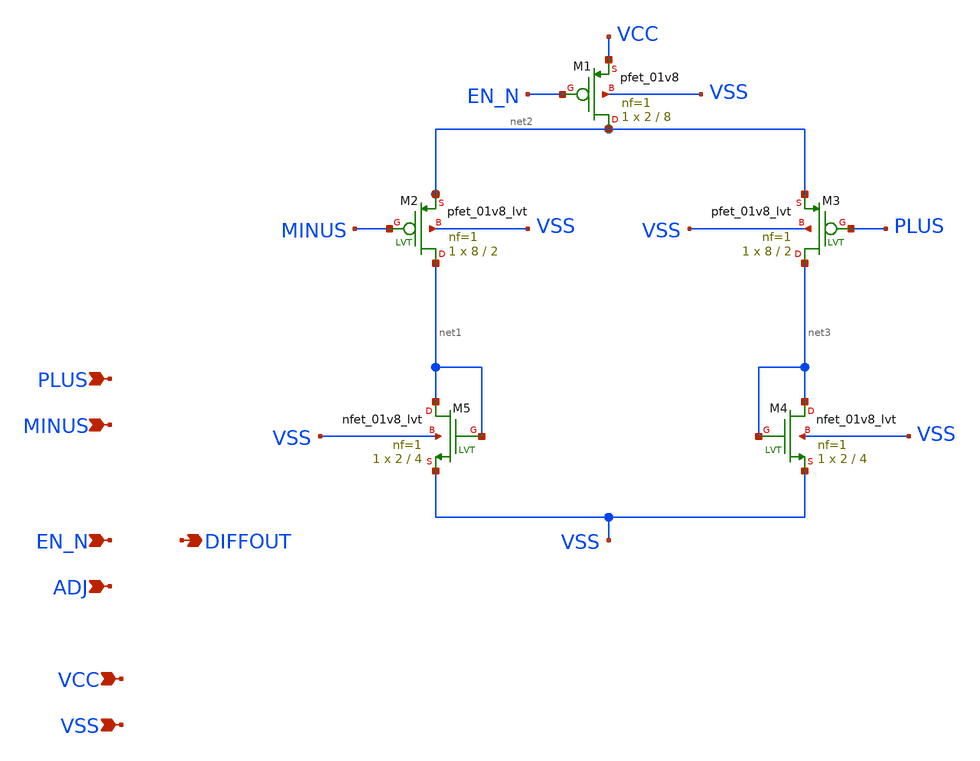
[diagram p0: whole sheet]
** sch_path: amplifier.sch
**.subckt amplifier PLUS MINUS VCC VSS EN_N ADJ DIFFOUT
*.ipin PLUS
*.ipin MINUS
*.ipin VCC
*.ipin VSS
*.ipin EN_N
*.ipin ADJ
*.opin DIFFOUT
XM1 net2 EN_N VCC VSS sky130_fd_pr__pfet_01v8 L=8 W=2 nf=1 ad='int((nf+1)/2) * W/nf * 0.29' as='int((nf+2)/2) * W/nf * 0.29'
+ pd='2*int((nf+1)/2) * (W/nf + 0.29)' ps='2*int((nf+2)/2) * (W/nf + 0.29)' nrd='0.29 / W' nrs='0.29 / W'
+ sa=0 sb=0 sd=0 mult=1 m=1
XM2 net1 MINUS net2 VSS sky130_fd_pr__pfet_01v8_lvt L=2 W=8 nf=1 ad='int((nf+1)/2) * W/nf * 0.29' as='int((nf+2)/2) * W/nf * 0.29'
+ pd='2*int((nf+1)/2) * (W/nf + 0.29)' ps='2*int((nf+2)/2) * (W/nf + 0.29)' nrd='0.29 / W' nrs='0.29 / W'
+ sa=0 sb=0 sd=0 mult=1 m=1
XM3 net3 PLUS net2 VSS sky130_fd_pr__pfet_01v8_lvt L=2 W=8 nf=1 ad='int((nf+1)/2) * W/nf * 0.29' as='int((nf+2)/2) * W/nf * 0.29'
+ pd='2*int((nf+1)/2) * (W/nf + 0.29)' ps='2*int((nf+2)/2) * (W/nf + 0.29)' nrd='0.29 / W' nrs='0.29 / W'
+ sa=0 sb=0 sd=0 mult=1 m=1
XM4 net3 net3 VSS VSS sky130_fd_pr__nfet_01v8_lvt L=4 W=2 nf=1 ad='int((nf+1)/2) * W/nf * 0.29' as='int((nf+2)/2) * W/nf * 0.29'
+ pd='2*int((nf+1)/2) * (W/nf + 0.29)' ps='2*int((nf+2)/2) * (W/nf + 0.29)' nrd='0.29 / W' nrs='0.29 / W'
+ sa=0 sb=0 sd=0 mult=1 m=1
XM5 net1 net1 VSS VSS sky130_fd_pr__nfet_01v8_lvt L=4 W=2 nf=1 ad='int((nf+1)/2) * W/nf * 0.29' as='int((nf+2)/2) * W/nf * 0.29'
+ pd='2*int((nf+1)/2) * (W/nf + 0.29)' ps='2*int((nf+2)/2) * (W/nf + 0.29)' nrd='0.29 / W' nrs='0.29 / W'
+ sa=0 sb=0 sd=0 mult=1 m=1
**.ends
.end
